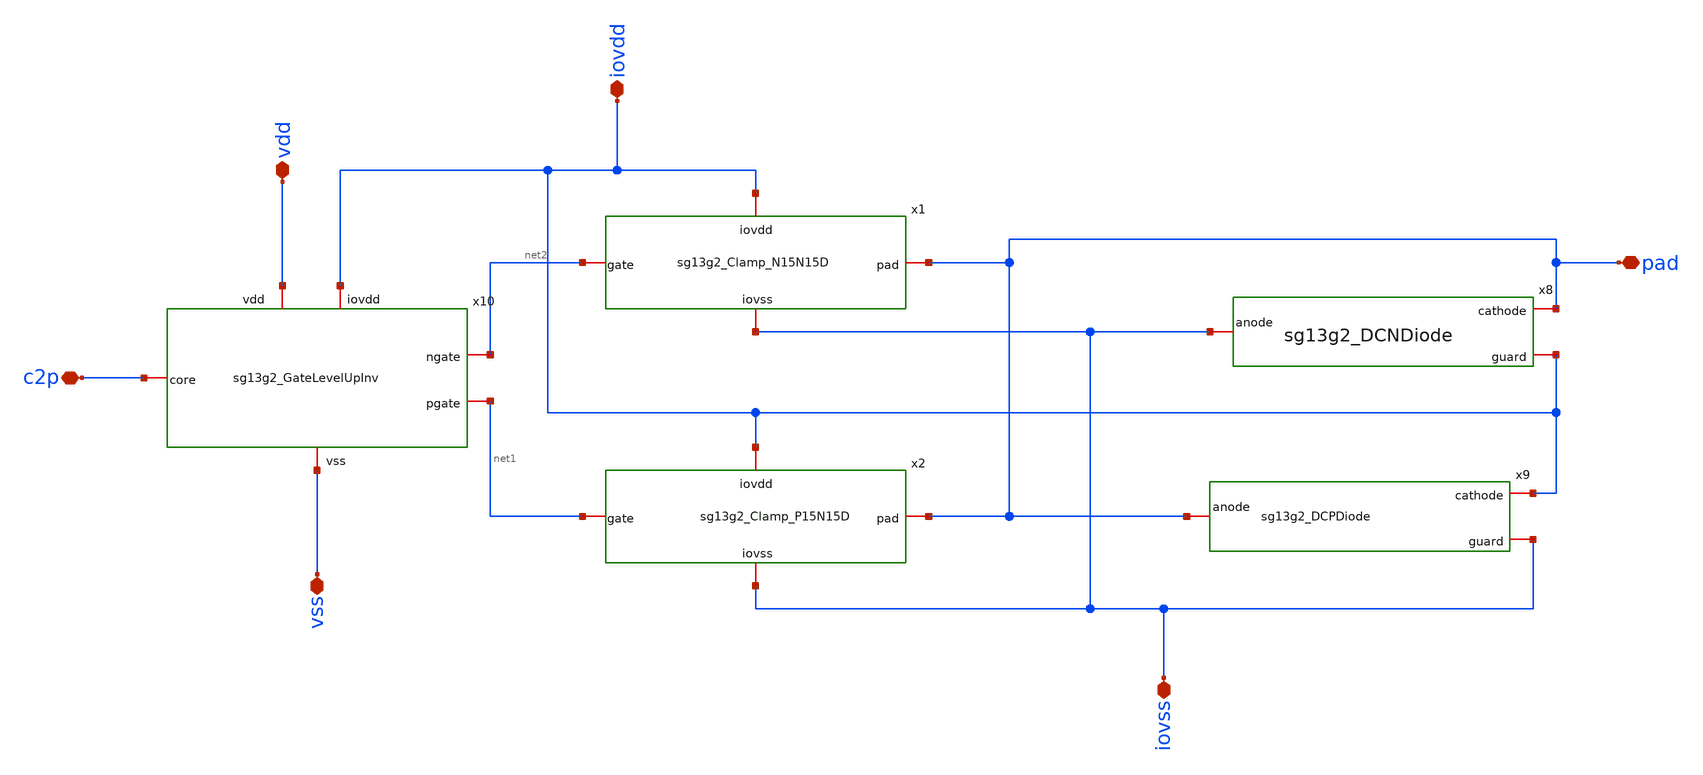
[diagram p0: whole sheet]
** sch_path: CDR4176-main/schematic/xschem/project_io/sg13g2_IOPadOut30mA/sg13g2_IOPadOut30mA.sch
**.subckt sg13g2_IOPadOut30mA iovss pad vss c2p vdd iovdd
*.iopin iovss
*.iopin pad
*.iopin vss
*.iopin c2p
*.iopin vdd
*.iopin iovdd
x1 iovdd pad net2 iovss sg13g2_Clamp_N15N15D
x2 iovdd net1 pad iovss sg13g2_Clamp_P15N15D
x8 pad iovss iovdd sg13g2_DCNDiode
x9 iovdd pad iovss sg13g2_DCPDiode
x10 vdd iovdd net2 net1 c2p vss sg13g2_GateLevelUpInv
**.ends
.end
